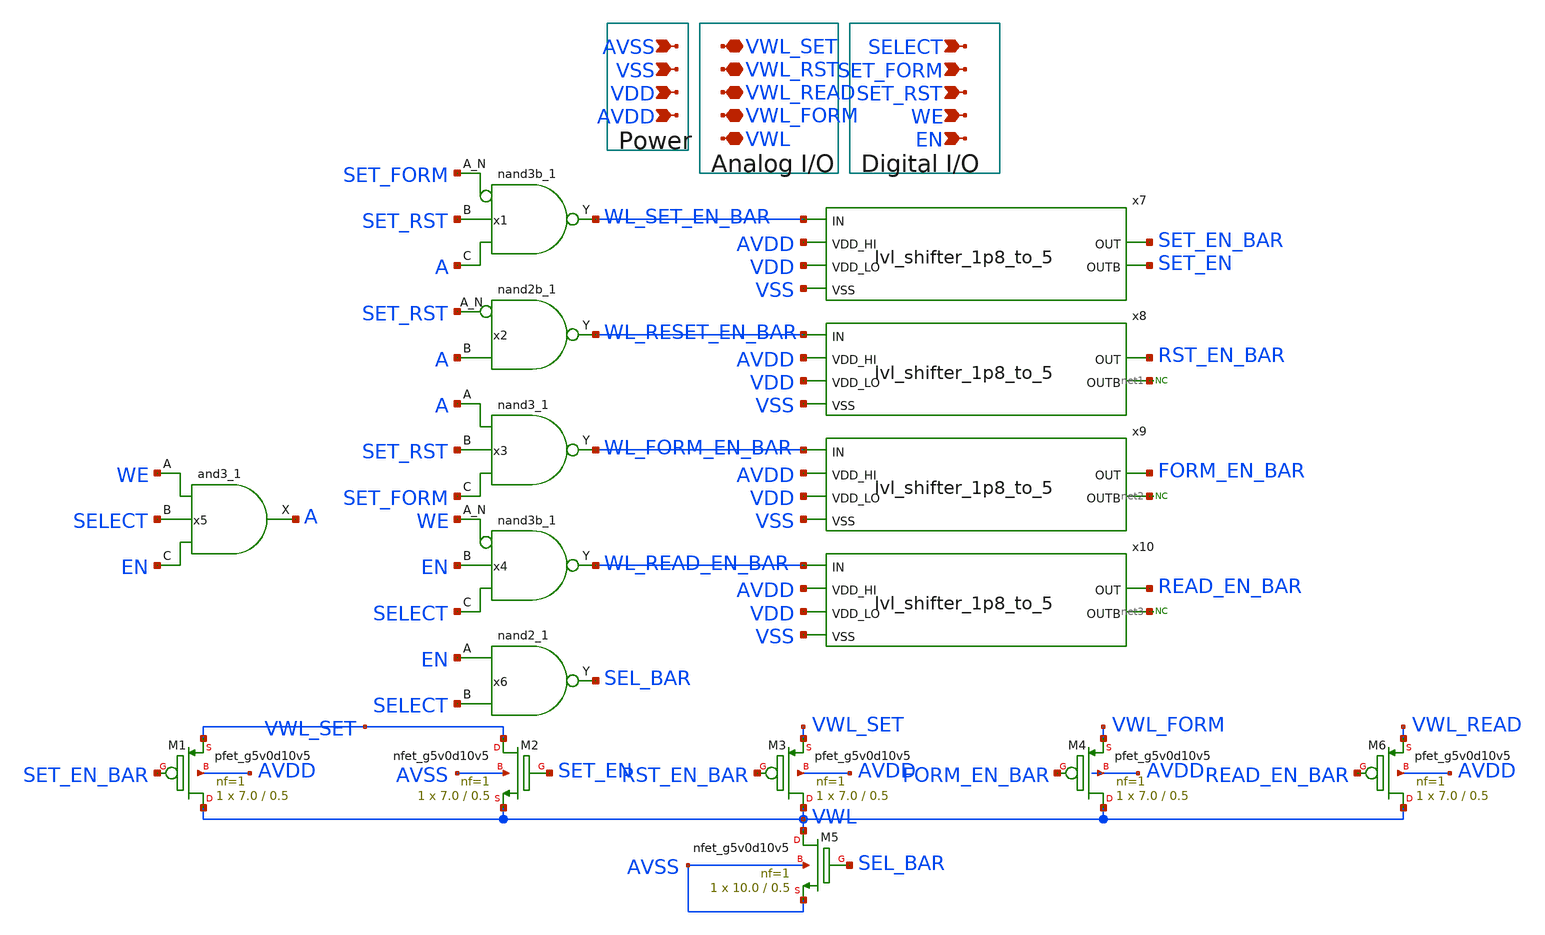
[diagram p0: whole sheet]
** sch_path: WL_Interface/WL_driver.sch
**.subckt WL_driver AVSS VSS VDD AVDD SELECT SET_FORM SET_RST WE EN VWL_SET VWL_RST VWL_READ
*+ VWL_FORM VWL
*.ipin AVSS
*.ipin VSS
*.ipin VDD
*.ipin AVDD
*.ipin SELECT
*.ipin SET_FORM
*.ipin SET_RST
*.ipin WE
*.ipin EN
*.iopin VWL_SET
*.iopin VWL_RST
*.iopin VWL_READ
*.iopin VWL_FORM
*.iopin VWL
x1 SET_FORM SET_RST A VSS VSS VDD VDD WL_SET_EN_BAR sky130_fd_sc_hd__nand3b_1
x2 SET_RST A VSS VSS VDD VDD WL_RESET_EN_BAR sky130_fd_sc_hd__nand2b_1
x3 A SET_RST SET_FORM VSS VSS VDD VDD WL_FORM_EN_BAR sky130_fd_sc_hd__nand3_1
x4 WE EN SELECT VSS VSS VDD VDD WL_READ_EN_BAR sky130_fd_sc_hd__nand3b_1
x5 WE SELECT EN VSS VSS VDD VDD A sky130_fd_sc_hd__and3_1
x6 EN SELECT VSS VSS VDD VDD SEL_BAR sky130_fd_sc_hd__nand2_1
XM1 VWL SET_EN_BAR VWL_SET AVDD sky130_fd_pr__pfet_g5v0d10v5 L=0.5 W=7.0 nf=1 ad='int((nf+1)/2) * W/nf * 0.29'
+ as='int((nf+2)/2) * W/nf * 0.29' pd='2*int((nf+1)/2) * (W/nf + 0.29)' ps='2*int((nf+2)/2) * (W/nf + 0.29)'
+ nrd='0.29 / W' nrs='0.29 / W' sa=0 sb=0 sd=0 mult=1 m=1
XM2 VWL_SET SET_EN VWL AVSS sky130_fd_pr__nfet_g5v0d10v5 L=0.5 W=7.0 nf=1 ad='int((nf+1)/2) * W/nf * 0.29'
+ as='int((nf+2)/2) * W/nf * 0.29' pd='2*int((nf+1)/2) * (W/nf + 0.29)' ps='2*int((nf+2)/2) * (W/nf + 0.29)'
+ nrd='0.29 / W' nrs='0.29 / W' sa=0 sb=0 sd=0 mult=1 m=1
XM3 VWL RST_EN_BAR VWL_SET AVDD sky130_fd_pr__pfet_g5v0d10v5 L=0.5 W=7.0 nf=1 ad='int((nf+1)/2) * W/nf * 0.29'
+ as='int((nf+2)/2) * W/nf * 0.29' pd='2*int((nf+1)/2) * (W/nf + 0.29)' ps='2*int((nf+2)/2) * (W/nf + 0.29)'
+ nrd='0.29 / W' nrs='0.29 / W' sa=0 sb=0 sd=0 mult=1 m=1
XM4 VWL FORM_EN_BAR VWL_FORM AVDD sky130_fd_pr__pfet_g5v0d10v5 L=0.5 W=7.0 nf=1 ad='int((nf+1)/2) * W/nf * 0.29'
+ as='int((nf+2)/2) * W/nf * 0.29' pd='2*int((nf+1)/2) * (W/nf + 0.29)' ps='2*int((nf+2)/2) * (W/nf + 0.29)'
+ nrd='0.29 / W' nrs='0.29 / W' sa=0 sb=0 sd=0 mult=1 m=1
XM5 VWL SEL_BAR AVSS AVSS sky130_fd_pr__nfet_g5v0d10v5 L=0.5 W=10.0 nf=1 ad='int((nf+1)/2) * W/nf * 0.29'
+ as='int((nf+2)/2) * W/nf * 0.29' pd='2*int((nf+1)/2) * (W/nf + 0.29)' ps='2*int((nf+2)/2) * (W/nf + 0.29)'
+ nrd='0.29 / W' nrs='0.29 / W' sa=0 sb=0 sd=0 mult=1 m=1
x7 AVDD SET_EN SET_EN_BAR VDD WL_SET_EN_BAR VSS lvl_shifter_1p8_to_5
x8 AVDD net1 RST_EN_BAR VDD WL_RESET_EN_BAR VSS lvl_shifter_1p8_to_5
x9 AVDD net2 FORM_EN_BAR VDD WL_FORM_EN_BAR VSS lvl_shifter_1p8_to_5
x10 AVDD net3 READ_EN_BAR VDD WL_READ_EN_BAR VSS lvl_shifter_1p8_to_5
* noconn #net1
* noconn #net2
* noconn #net3
XM6 VWL READ_EN_BAR VWL_READ AVDD sky130_fd_pr__pfet_g5v0d10v5 L=0.5 W=7.0 nf=1 ad='int((nf+1)/2) * W/nf * 0.29'
+ as='int((nf+2)/2) * W/nf * 0.29' pd='2*int((nf+1)/2) * (W/nf + 0.29)' ps='2*int((nf+2)/2) * (W/nf + 0.29)'
+ nrd='0.29 / W' nrs='0.29 / W' sa=0 sb=0 sd=0 mult=1 m=1
**.ends

* expanding   symbol:  BL_SL_Writing_Interface/lvl_shifter_1p8_to_5.sym # of pins=6
** sym_path: BL_SL_Writing_Interface/lvl_shifter_1p8_to_5.sym
** sch_path: BL_SL_Writing_Interface/lvl_shifter_1p8_to_5.sch
.subckt lvl_shifter_1p8_to_5 VDD_HI OUTB OUT VDD_LO IN VSS
*.ipin VDD_HI
*.opin OUT
*.opin OUTB
*.ipin IN
*.ipin VDD_LO
*.ipin VSS
XM5 net1 IN VSS VSS sky130_fd_pr__nfet_01v8 L=0.15 W=0.42 nf=1 ad='int((nf+1)/2) * W/nf * 0.29' as='int((nf+2)/2) * W/nf * 0.29'
+ pd='2*int((nf+1)/2) * (W/nf + 0.29)' ps='2*int((nf+2)/2) * (W/nf + 0.29)' nrd='0.29 / W' nrs='0.29 / W'
+ sa=0 sb=0 sd=0 mult=1 m=1
XM7 net2 net1 VSS VSS sky130_fd_pr__nfet_01v8 L=0.15 W=0.42 nf=1 ad='int((nf+1)/2) * W/nf * 0.29' as='int((nf+2)/2) * W/nf * 0.29'
+ pd='2*int((nf+1)/2) * (W/nf + 0.29)' ps='2*int((nf+2)/2) * (W/nf + 0.29)' nrd='0.29 / W' nrs='0.29 / W'
+ sa=0 sb=0 sd=0 mult=1 m=1
XM3 net1 IN VDD_LO VDD_LO sky130_fd_pr__pfet_01v8 L=0.15 W=0.84 nf=1 ad='int((nf+1)/2) * W/nf * 0.29'
+ as='int((nf+2)/2) * W/nf * 0.29' pd='2*int((nf+1)/2) * (W/nf + 0.29)' ps='2*int((nf+2)/2) * (W/nf + 0.29)'
+ nrd='0.29 / W' nrs='0.29 / W' sa=0 sb=0 sd=0 mult=1 m=1
XM4 net2 net1 VDD_LO VDD_LO sky130_fd_pr__pfet_01v8 L=0.15 W=0.84 nf=1 ad='int((nf+1)/2) * W/nf * 0.29'
+ as='int((nf+2)/2) * W/nf * 0.29' pd='2*int((nf+1)/2) * (W/nf + 0.29)' ps='2*int((nf+2)/2) * (W/nf + 0.29)'
+ nrd='0.29 / W' nrs='0.29 / W' sa=0 sb=0 sd=0 mult=1 m=1
XM6 OUT net1 VSS VSS sky130_fd_pr__nfet_g5v0d10v5 L=0.5 W=5 nf=1 ad='int((nf+1)/2) * W/nf * 0.29' as='int((nf+2)/2) * W/nf * 0.29'
+ pd='2*int((nf+1)/2) * (W/nf + 0.29)' ps='2*int((nf+2)/2) * (W/nf + 0.29)' nrd='0.29 / W' nrs='0.29 / W'
+ sa=0 sb=0 sd=0 mult=1 m=1
XM8 OUTB net2 VSS VSS sky130_fd_pr__nfet_g5v0d10v5 L=0.5 W=5 nf=1 ad='int((nf+1)/2) * W/nf * 0.29' as='int((nf+2)/2) * W/nf * 0.29'
+ pd='2*int((nf+1)/2) * (W/nf + 0.29)' ps='2*int((nf+2)/2) * (W/nf + 0.29)' nrd='0.29 / W' nrs='0.29 / W'
+ sa=0 sb=0 sd=0 mult=1 m=1
XM1 OUT OUTB VDD_HI VDD_HI sky130_fd_pr__pfet_g5v0d10v5 L=0.5 W=1.5 nf=1 ad='int((nf+1)/2) * W/nf * 0.29'
+ as='int((nf+2)/2) * W/nf * 0.29' pd='2*int((nf+1)/2) * (W/nf + 0.29)' ps='2*int((nf+2)/2) * (W/nf + 0.29)'
+ nrd='0.29 / W' nrs='0.29 / W' sa=0 sb=0 sd=0 mult=1 m=1
XM2 OUTB OUT VDD_HI VDD_HI sky130_fd_pr__pfet_g5v0d10v5 L=0.5 W=1.5 nf=1 ad='int((nf+1)/2) * W/nf * 0.29'
+ as='int((nf+2)/2) * W/nf * 0.29' pd='2*int((nf+1)/2) * (W/nf + 0.29)' ps='2*int((nf+2)/2) * (W/nf + 0.29)'
+ nrd='0.29 / W' nrs='0.29 / W' sa=0 sb=0 sd=0 mult=1 m=1
.ends

.end
